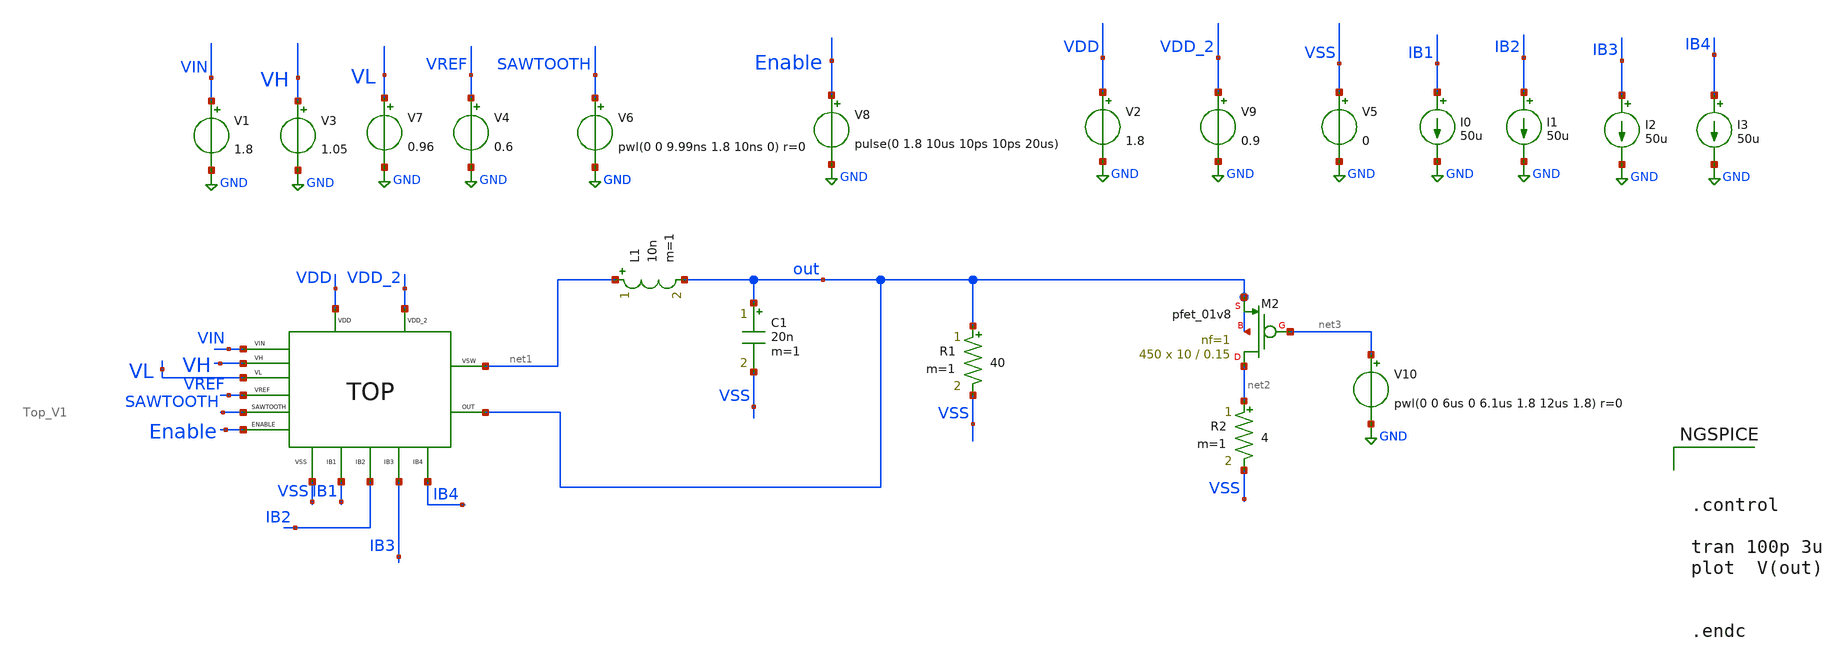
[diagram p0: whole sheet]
** sch_path: xschem/DC_DC_Converter_xschem/OTHERS/DC_DC_Converter_JV8/TOP_LEVEL/Top_Final/Top_TB.sch
**.subckt Top_TB
V1 VIN GND 1.8
I0 IB1 GND 50u
V2 VDD GND 1.8
V5 VSS GND 0
V4 VREF GND 0.6
I1 IB2 GND 50u
V6 SAWTOOTH GND pwl(0 0 9.99ns 1.8 10ns 0) r=0
V3 VH GND 1.05
V7 VL GND 0.96
I2 IB3 GND 50u
I3 IB4 GND 50u
V8 Enable GND pulse(0 1.8 10us 10ps 10ps 20us)
L1 net1 out 10n m=1
C1 out VSS 20n m=1
XM2 net2 net3 out out sky130_fd_pr__pfet_01v8 L=0.15 W=10 nf=1 ad='int((nf+1)/2) * W/nf * 0.29' as='int((nf+2)/2) * W/nf * 0.29'
+ pd='2*int((nf+1)/2) * (W/nf + 0.29)' ps='2*int((nf+2)/2) * (W/nf + 0.29)' nrd='0.29 / W' nrs='0.29 / W'
+ sa=0 sb=0 sd=0 mult=450 m=450
V10 net3 GND pwl(0 0 6us 0 6.1us 1.8 12us 1.8) r=0
R1 out VSS 40 m=1
R2 net2 VSS 4 m=1
x1 VDD VDD_2 net1 out VIN VREF Enable VSS IB1 IB2 VH VL IB3 IB4 SAWTOOTH Top_V1
V9 VDD_2 GND 0.9
**** begin user architecture code

** opencircuitdesign pdks install
.lib $::SKYWATER_MODELS/sky130.lib.spice tt





.control

tran 100p 3u
plot  V(out)


.endc


**** end user architecture code
**.ends
.GLOBAL GND
.end
